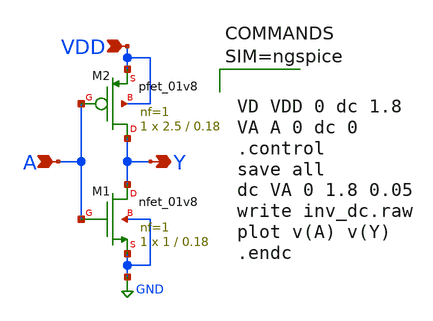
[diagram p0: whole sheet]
** sch_path: inv_dc.sch
**.subckt inv_dc A VDD Y
*.ipin A
*.ipin VDD
*.opin Y
XM1 Y A GND GND sky130_fd_pr__nfet_01v8 L=0.18 W=1 nf=1 ad='int((nf+1)/2) * W/nf * 0.29' as='int((nf+2)/2) * W/nf * 0.29'
+ pd='2*int((nf+1)/2) * (W/nf + 0.29)' ps='2*int((nf+2)/2) * (W/nf + 0.29)' nrd='0.29 / W' nrs='0.29 / W'
+ sa=0 sb=0 sd=0 mult=1 m=1
XM2 Y A VDD VDD sky130_fd_pr__pfet_01v8 L=0.18 W=2.5 nf=1 ad='int((nf+1)/2) * W/nf * 0.29' as='int((nf+2)/2) * W/nf * 0.29'
+ pd='2*int((nf+1)/2) * (W/nf + 0.29)' ps='2*int((nf+2)/2) * (W/nf + 0.29)' nrd='0.29 / W' nrs='0.29 / W'
+ sa=0 sb=0 sd=0 mult=1 m=1
**** begin user architecture code

** opencircuitdesign pdks install
.lib $::SKYWATER_MODELS/sky130.lib.spice tt





VD VDD 0 dc 1.8
VA A 0 dc 0
.control
save all
dc VA 0 1.8 0.05
write inv_dc.raw
plot v(A) v(Y)
.endc



**** end user architecture code
**.ends
.GLOBAL GND
.end
